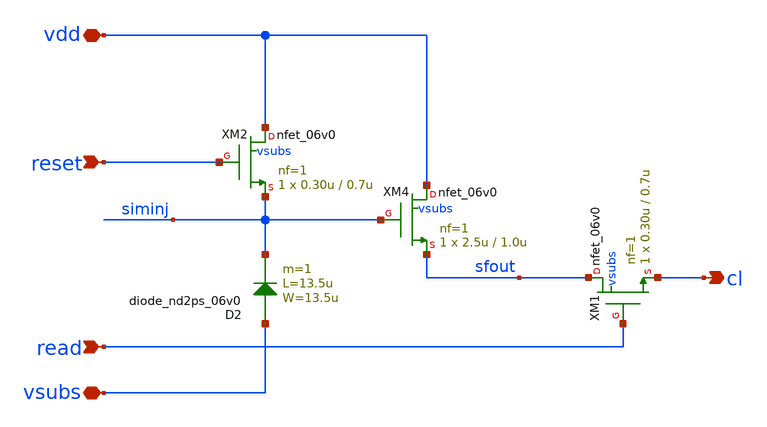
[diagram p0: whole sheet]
** sch_path: xschem/ip_pixel_nd2ps.sch
**.subckt ip_pixel_nd2ps vdd vsubs reset read cl
*.iopin vdd
*.iopin vsubs
*.ipin reset
*.ipin read
*.opin cl
D2 vsubs siminj diode_nd2ps_06v0 area='13.5u * 13.5u ' pj='2*13.5u + 2*13.5u ' m=1
XM4 vdd siminj sfout vsubs nfet_06v0 L=1.0u W=2.5u nf=1 ad='int((nf+1)/2) * W/nf * 0.18u' as='int((nf+2)/2) * W/nf * 0.18u'
+ pd='2*int((nf+1)/2) * (W/nf + 0.18u)' ps='2*int((nf+2)/2) * (W/nf + 0.18u)' nrd='0.18u / W' nrs='0.18u / W'
+ sa=0 sb=0 sd=0 m=1 par=1
XM2 vdd reset siminj vsubs nfet_06v0 L=0.7u W=0.30u nf=1 ad='int((nf+1)/2) * W/nf * 0.18u' as='int((nf+2)/2) * W/nf * 0.18u'
+ pd='2*int((nf+1)/2) * (W/nf + 0.18u)' ps='2*int((nf+2)/2) * (W/nf + 0.18u)' nrd='0.18u / W' nrs='0.18u / W'
+ sa=0 sb=0 sd=0 m=1 par=1
XM1 sfout read cl vsubs nfet_06v0 L=0.7u W=0.30u nf=1 ad='int((nf+1)/2) * W/nf * 0.18u' as='int((nf+2)/2) * W/nf * 0.18u'
+ pd='2*int((nf+1)/2) * (W/nf + 0.18u)' ps='2*int((nf+2)/2) * (W/nf + 0.18u)' nrd='0.18u / W' nrs='0.18u / W'
+ sa=0 sb=0 sd=0 m=1 par=1
**.ends
.end
